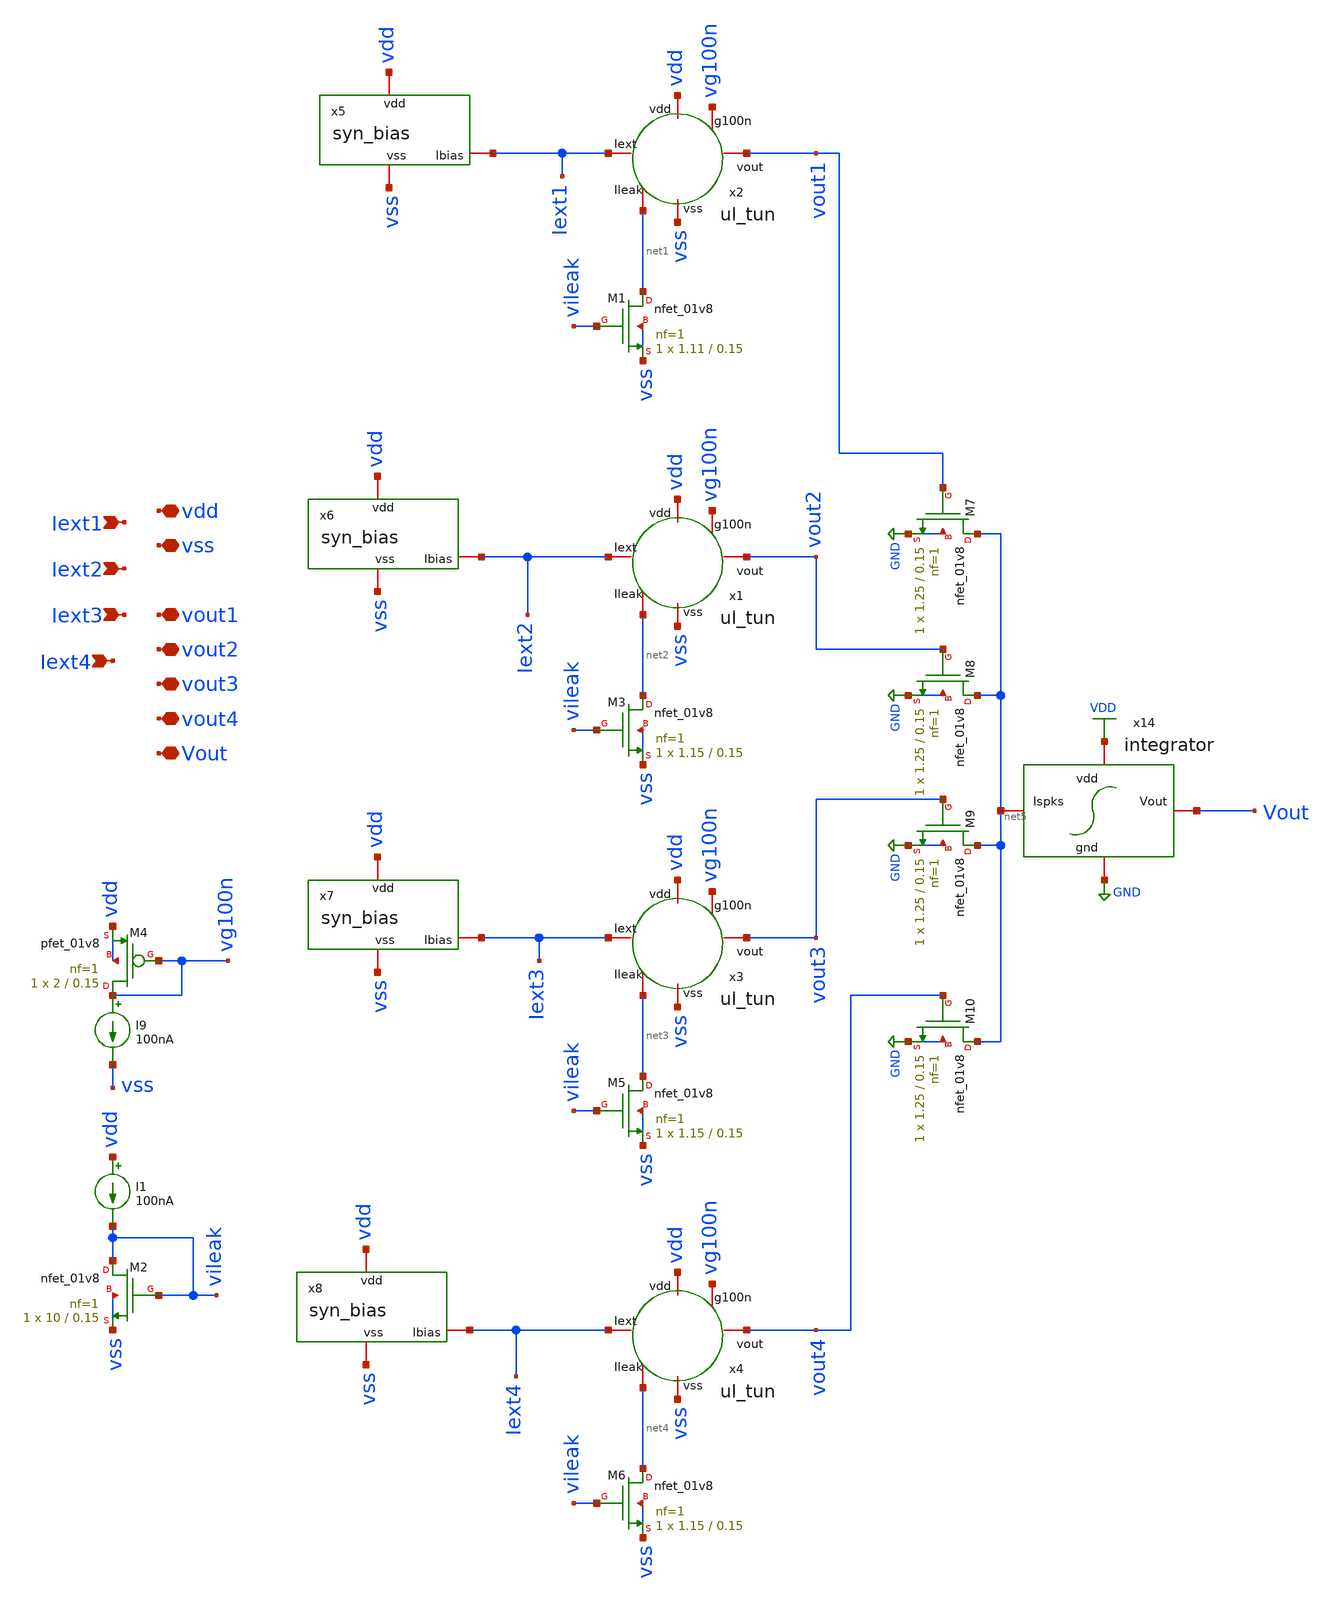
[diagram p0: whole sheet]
** sch_path: layer/layer_output.sch
**.subckt layer_output vdd vss Iext1 Vout Iext2 Iext3 Iext4 vout1 vout2 vout3 vout4
*.iopin vdd
*.iopin vss
*.ipin Iext1
*.iopin Vout
*.ipin Iext2
*.ipin Iext3
*.ipin Iext4
*.iopin vout1
*.iopin vout2
*.iopin vout3
*.iopin vout4
x2 Iext1 vdd vg100n vout1 net1 vss ul_tun
I9 vg100n vss 100nA
XM4 vg100n vg100n vdd vdd sky130_fd_pr__pfet_01v8 L=0.15 W=2 nf=1 ad='int((nf+1)/2) * W/nf * 0.29' as='int((nf+2)/2) * W/nf * 0.29'
+ pd='2*int((nf+1)/2) * (W/nf + 0.29)' ps='2*int((nf+2)/2) * (W/nf + 0.29)' nrd='0.29 / W' nrs='0.29 / W'
+ sa=0 sb=0 sd=0 mult=1 m=1
XM1 net1 vileak vss vss sky130_fd_pr__nfet_01v8 L=0.15 W=1.11 nf=1 ad='int((nf+1)/2) * W/nf * 0.29' as='int((nf+2)/2) * W/nf * 0.29'
+ pd='2*int((nf+1)/2) * (W/nf + 0.29)' ps='2*int((nf+2)/2) * (W/nf + 0.29)' nrd='0.29 / W' nrs='0.29 / W'
+ sa=0 sb=0 sd=0 mult=1 m=1
XM2 vileak vileak vss vss sky130_fd_pr__nfet_01v8 L=0.15 W=10 nf=1 ad='int((nf+1)/2) * W/nf * 0.29' as='int((nf+2)/2) * W/nf * 0.29'
+ pd='2*int((nf+1)/2) * (W/nf + 0.29)' ps='2*int((nf+2)/2) * (W/nf + 0.29)' nrd='0.29 / W' nrs='0.29 / W'
+ sa=0 sb=0 sd=0 mult=1 m=1
I1 vdd vileak 100nA
x1 Iext2 vdd vg100n vout2 net2 vss ul_tun
XM3 net2 vileak vss vss sky130_fd_pr__nfet_01v8 L=0.15 W=1.15 nf=1 ad='int((nf+1)/2) * W/nf * 0.29' as='int((nf+2)/2) * W/nf * 0.29'
+ pd='2*int((nf+1)/2) * (W/nf + 0.29)' ps='2*int((nf+2)/2) * (W/nf + 0.29)' nrd='0.29 / W' nrs='0.29 / W'
+ sa=0 sb=0 sd=0 mult=1 m=1
x3 Iext3 vdd vg100n vout3 net3 vss ul_tun
XM5 net3 vileak vss vss sky130_fd_pr__nfet_01v8 L=0.15 W=1.15 nf=1 ad='int((nf+1)/2) * W/nf * 0.29' as='int((nf+2)/2) * W/nf * 0.29'
+ pd='2*int((nf+1)/2) * (W/nf + 0.29)' ps='2*int((nf+2)/2) * (W/nf + 0.29)' nrd='0.29 / W' nrs='0.29 / W'
+ sa=0 sb=0 sd=0 mult=1 m=1
x4 Iext4 vdd vg100n vout4 net4 vss ul_tun
XM6 net4 vileak vss vss sky130_fd_pr__nfet_01v8 L=0.15 W=1.15 nf=1 ad='int((nf+1)/2) * W/nf * 0.29' as='int((nf+2)/2) * W/nf * 0.29'
+ pd='2*int((nf+1)/2) * (W/nf + 0.29)' ps='2*int((nf+2)/2) * (W/nf + 0.29)' nrd='0.29 / W' nrs='0.29 / W'
+ sa=0 sb=0 sd=0 mult=1 m=1
x14 VDD Vout net5 GND integrator
XM7 net5 vout1 GND GND sky130_fd_pr__nfet_01v8 L=0.15 W=1.25 nf=1 ad='int((nf+1)/2) * W/nf * 0.29' as='int((nf+2)/2) * W/nf * 0.29'
+ pd='2*int((nf+1)/2) * (W/nf + 0.29)' ps='2*int((nf+2)/2) * (W/nf + 0.29)' nrd='0.29 / W' nrs='0.29 / W'
+ sa=0 sb=0 sd=0 mult=1 m=1
XM8 net5 vout2 GND GND sky130_fd_pr__nfet_01v8 L=0.15 W=1.25 nf=1 ad='int((nf+1)/2) * W/nf * 0.29' as='int((nf+2)/2) * W/nf * 0.29'
+ pd='2*int((nf+1)/2) * (W/nf + 0.29)' ps='2*int((nf+2)/2) * (W/nf + 0.29)' nrd='0.29 / W' nrs='0.29 / W'
+ sa=0 sb=0 sd=0 mult=1 m=1
XM9 net5 vout3 GND GND sky130_fd_pr__nfet_01v8 L=0.15 W=1.25 nf=1 ad='int((nf+1)/2) * W/nf * 0.29' as='int((nf+2)/2) * W/nf * 0.29'
+ pd='2*int((nf+1)/2) * (W/nf + 0.29)' ps='2*int((nf+2)/2) * (W/nf + 0.29)' nrd='0.29 / W' nrs='0.29 / W'
+ sa=0 sb=0 sd=0 mult=1 m=1
XM10 net5 vout4 GND GND sky130_fd_pr__nfet_01v8 L=0.15 W=1.25 nf=1 ad='int((nf+1)/2) * W/nf * 0.29' as='int((nf+2)/2) * W/nf * 0.29'
+ pd='2*int((nf+1)/2) * (W/nf + 0.29)' ps='2*int((nf+2)/2) * (W/nf + 0.29)' nrd='0.29 / W' nrs='0.29 / W'
+ sa=0 sb=0 sd=0 mult=1 m=1
x5 vdd vss Iext1 syn_bias
x6 vdd vss Iext2 syn_bias
x7 vdd vss Iext3 syn_bias
x8 vdd vss Iext4 syn_bias
**.ends

* expanding   symbol:  Neuron/ultralif/ul_tun.sym # of pins=6
** sym_path: Neuron/ultralif/ul_tun.sym
** sch_path: Neuron/ultralif/ul_tun.sch
.subckt ul_tun Iext vdd g100n vout Ileak vss
*.iopin Iext
*.iopin vout
*.iopin vss
*.iopin Ileak
*.iopin vdd
*.iopin g100n
XM1 Ileak Ileak net1 vdd sky130_fd_pr__pfet_01v8 L=10 W=1 nf=1 ad='int((nf+1)/2) * W/nf * 0.29' as='int((nf+2)/2) * W/nf * 0.29'
+ pd='2*int((nf+1)/2) * (W/nf + 0.29)' ps='2*int((nf+2)/2) * (W/nf + 0.29)' nrd='0.29 / W' nrs='0.29 / W'
+ sa=0 sb=0 sd=0 mult=1 m=1
XM2 Ileak net2 net1 vdd sky130_fd_pr__pfet_01v8 L=0.15 W=1.5 nf=1 ad='int((nf+1)/2) * W/nf * 0.29' as='int((nf+2)/2) * W/nf * 0.29'
+ pd='2*int((nf+1)/2) * (W/nf + 0.29)' ps='2*int((nf+2)/2) * (W/nf + 0.29)' nrd='0.29 / W' nrs='0.29 / W'
+ sa=0 sb=0 sd=0 mult=1 m=1
XM3 net2 net2 net1 vdd sky130_fd_pr__pfet_01v8 L=0.15 W=15 nf=1 ad='int((nf+1)/2) * W/nf * 0.29' as='int((nf+2)/2) * W/nf * 0.29'
+ pd='2*int((nf+1)/2) * (W/nf + 0.29)' ps='2*int((nf+2)/2) * (W/nf + 0.29)' nrd='0.29 / W' nrs='0.29 / W'
+ sa=0 sb=0 sd=0 mult=1 m=1
XM4 net2 Ileak vss vss sky130_fd_pr__nfet_01v8 L=4 W=1 nf=1 ad='int((1 + 1)/2) * 1 / 1 * 0.29' as='int((1 + 2)/2) * 1 / 1 * 0.29'
+ pd='2*int((1 + 1)/2) * (1 / 1 + 0.29)' ps='2*int((1 + 2)/2) * (1 / 1 + 0.29)' nrd='0.29 / 1 ' nrs='0.29 / 1 '
+ sa=0 sb=0 sd=0 mult=1 m=1
C1 net1 vss 1p m=1
XM5 vout_n Ileak vss vss sky130_fd_pr__nfet_01v8 L=0.15 W=1 nf=1 ad='int((1 + 1)/2) * 1 / 1 * 0.29' as='int((1 + 2)/2) * 1 / 1 * 0.29'
+ pd='2*int((1 + 1)/2) * (1 / 1 + 0.29)' ps='2*int((1 + 2)/2) * (1 / 1 + 0.29)' nrd='0.29 / 1 ' nrs='0.29 / 1 '
+ sa=0 sb=0 sd=0 mult=1 m=1
XM6 vout_n g100n vdd vdd sky130_fd_pr__pfet_01v8 L=0.15 W=2 nf=1 ad='int((nf+1)/2) * W/nf * 0.29' as='int((nf+2)/2) * W/nf * 0.29'
+ pd='2*int((nf+1)/2) * (W/nf + 0.29)' ps='2*int((nf+2)/2) * (W/nf + 0.29)' nrd='0.29 / W' nrs='0.29 / W'
+ sa=0 sb=0 sd=0 mult=1 m=1
XM7 vout vout_n vss vss sky130_fd_pr__nfet_01v8 L=0.15 W=1 nf=1 ad='int((1 + 1)/2) * 1 / 1 * 0.29' as='int((1 + 2)/2) * 1 / 1 * 0.29'
+ pd='2*int((1 + 1)/2) * (1 / 1 + 0.29)' ps='2*int((1 + 2)/2) * (1 / 1 + 0.29)' nrd='0.29 / 1 ' nrs='0.29 / 1 '
+ sa=0 sb=0 sd=0 mult=1 m=1
XM8 vout vout_n vdd vdd sky130_fd_pr__pfet_01v8 L=0.15 W=2 nf=1 ad='int((nf+1)/2) * W/nf * 0.29' as='int((nf+2)/2) * W/nf * 0.29'
+ pd='2*int((nf+1)/2) * (W/nf + 0.29)' ps='2*int((nf+2)/2) * (W/nf + 0.29)' nrd='0.29 / W' nrs='0.29 / W'
+ sa=0 sb=0 sd=0 mult=1 m=1
vext Iext net1 0
**** begin user architecture code


.save i(vext)


**** end user architecture code
.ends


* expanding   symbol:  Neuron/ultralif/integrator.sym # of pins=4
** sym_path: Neuron/ultralif/integrator.sym
** sch_path: Neuron/ultralif/integrator.sch
.subckt integrator vdd Vout Ispks gnd
*.iopin Ispks
*.iopin Vout
*.iopin vdd
*.iopin gnd
XMIn Ispks vx vsyn vdd sky130_fd_pr__pfet_01v8 L=0.15 W=5 nf=1 ad='int((nf+1)/2) * W/nf * 0.29' as='int((nf+2)/2) * W/nf * 0.29'
+ pd='2*int((nf+1)/2) * (W/nf + 0.29)' ps='2*int((nf+2)/2) * (W/nf + 0.29)' nrd='0.29 / W' nrs='0.29 / W'
+ sa=0 sb=0 sd=0 mult=1 m=1
XM3 vsyn vdd vdd vdd sky130_fd_pr__pfet_01v8 L=0.15 W=50 nf=1 ad='int((nf+1)/2) * W/nf * 0.29' as='int((nf+2)/2) * W/nf * 0.29'
+ pd='2*int((nf+1)/2) * (W/nf + 0.29)' ps='2*int((nf+2)/2) * (W/nf + 0.29)' nrd='0.29 / W' nrs='0.29 / W'
+ sa=0 sb=0 sd=0 mult=1 m=1
XM4 Vout vsyn vdd vdd sky130_fd_pr__pfet_01v8 L=0.15 W=50 nf=1 ad='int((nf+1)/2) * W/nf * 0.29' as='int((nf+2)/2) * W/nf * 0.29'
+ pd='2*int((nf+1)/2) * (W/nf + 0.29)' ps='2*int((nf+2)/2) * (W/nf + 0.29)' nrd='0.29 / W' nrs='0.29 / W'
+ sa=0 sb=0 sd=0 mult=1 m=1
XCsyn vdd vsyn sky130_fd_pr__cap_mim_m3_1 W=22.2 L=22.2 MF=1 m=1
XR2 vx vdd sky130_fd_pr__res_generic_po W=1 L=1 m=1
XR1 gnd vx sky130_fd_pr__res_generic_po W=1 L=1 m=1
XM6 Vout vx gnd gnd sky130_fd_pr__nfet_01v8 L=0.15 W=0.5 nf=1 ad='int((nf+1)/2) * W/nf * 0.29' as='int((nf+2)/2) * W/nf * 0.29'
+ pd='2*int((nf+1)/2) * (W/nf + 0.29)' ps='2*int((nf+2)/2) * (W/nf + 0.29)' nrd='0.29 / W' nrs='0.29 / W'
+ sa=0 sb=0 sd=0 mult=1 m=1
.ends


* expanding   symbol:  /foss/designs/SNN_IPN/Neuron/ultralif/syn_bias.sym # of pins=3
** sym_path: Neuron/ultralif/syn_bias.sym
** sch_path: Neuron/ultralif/syn_bias.sch
.subckt syn_bias vdd vss Ibias
*.iopin vss
*.iopin vdd
*.iopin Ibias
XM2 Ibias net1 vdd vdd sky130_fd_pr__pfet_01v8 L=1 W=0.5 nf=1 ad='int((nf+1)/2) * W/nf * 0.29' as='int((nf+2)/2) * W/nf * 0.29'
+ pd='2*int((nf+1)/2) * (W/nf + 0.29)' ps='2*int((nf+2)/2) * (W/nf + 0.29)' nrd='0.29 / W' nrs='0.29 / W'
+ sa=0 sb=0 sd=0 mult=1 m=1
XR1 net1 vdd sky130_fd_pr__res_generic_po W=1.15 L=1 m=1
XR2 vss net1 sky130_fd_pr__res_generic_po W=1 L=1 m=1
.ends

.GLOBAL GND
.GLOBAL VDD
.end
